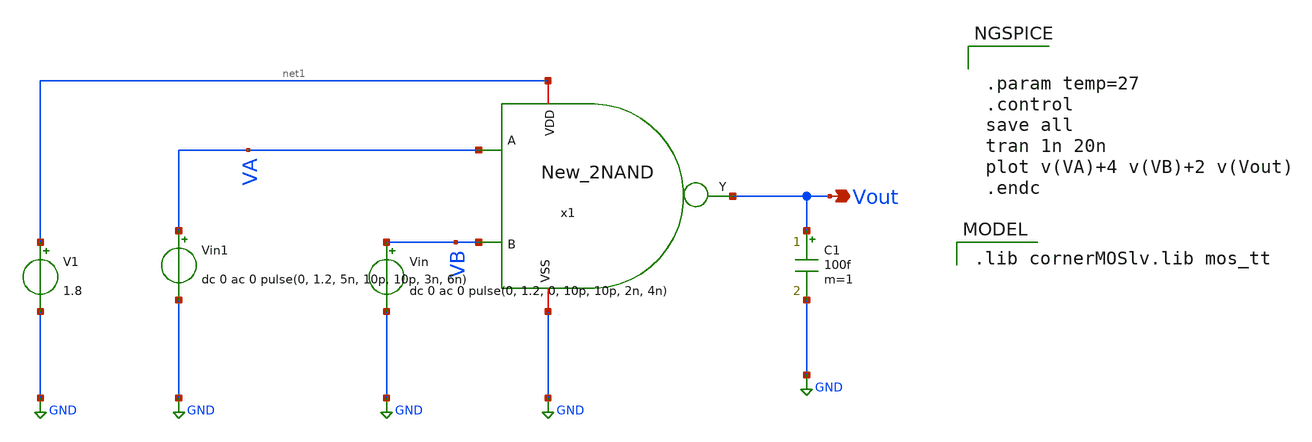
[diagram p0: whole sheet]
** sch_path: Team 1 Design/design_data/xschem/2_Input_NAND_New/New_2NAND_tb.sch
**.subckt New_2NAND_tb Vout
*.opin Vout
Vin VB GND dc 0 ac 0 pulse(0, 1.2, 0, 10p, 10p, 2n, 4n)
Vin1 VA GND dc 0 ac 0 pulse(0, 1.2, 5n, 10p, 10p, 3n, 6n)
C1 Vout GND 100f m=1
V1 net1 GND 1.8
x1 net1 GND VA Vout VB New_2NAND
**** begin user architecture code
 .lib cornerMOSlv.lib mos_tt



.param temp=27
.control
save all
tran 1n 20n
plot v(VA)+4 v(VB)+2 v(Vout)
.endc


**** end user architecture code
**.ends
.GLOBAL GND
.end
